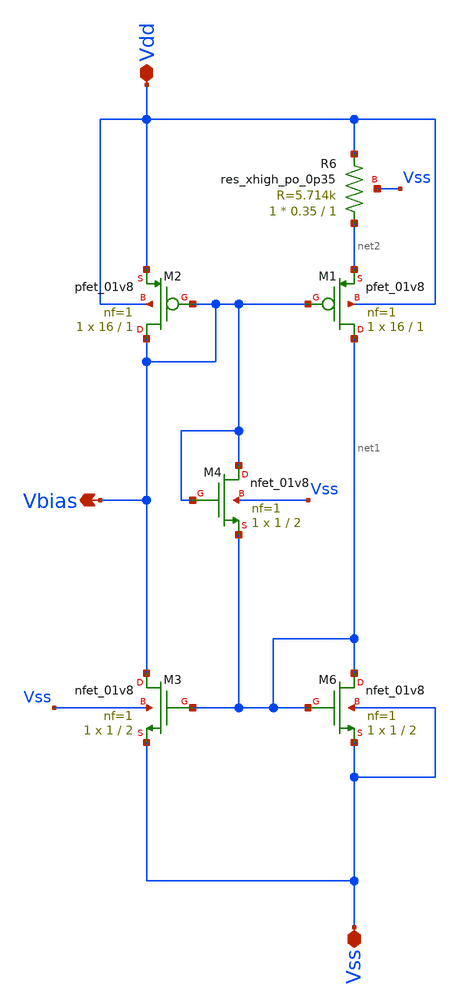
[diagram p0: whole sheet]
** sch_path: Circuits/Examples/OpAmp/GmBiasP.sch
**.subckt GmBiasP Vss Vdd Vbias
*.iopin Vss
*.iopin Vdd
*.opin Vbias
XM6 net1 net1 Vss Vss sky130_fd_pr__nfet_01v8 L=2 W=1 nf=1 ad='int((nf+1)/2) * W/nf * 0.29' as='int((nf+2)/2) * W/nf * 0.29'
+ pd='2*int((nf+1)/2) * (W/nf + 0.29)' ps='2*int((nf+2)/2) * (W/nf + 0.29)' nrd='0.29 / W' nrs='0.29 / W'
+ sa=0 sb=0 sd=0 mult=1 m=1
XM2 Vbias Vbias Vdd Vdd sky130_fd_pr__pfet_01v8 L=1 W=16 nf=1 ad='int((nf+1)/2) * W/nf * 0.29' as='int((nf+2)/2) * W/nf * 0.29'
+ pd='2*int((nf+1)/2) * (W/nf + 0.29)' ps='2*int((nf+2)/2) * (W/nf + 0.29)' nrd='0.29 / W' nrs='0.29 / W'
+ sa=0 sb=0 sd=0 mult=1 m=1
XM1 net1 Vbias net2 Vdd sky130_fd_pr__pfet_01v8 L=1 W=16 nf=1 ad='int((nf+1)/2) * W/nf * 0.29' as='int((nf+2)/2) * W/nf * 0.29'
+ pd='2*int((nf+1)/2) * (W/nf + 0.29)' ps='2*int((nf+2)/2) * (W/nf + 0.29)' nrd='0.29 / W' nrs='0.29 / W'
+ sa=0 sb=0 sd=0 mult=1 m=1
XM3 Vbias net1 Vss Vss sky130_fd_pr__nfet_01v8 L=2 W=1 nf=1 ad='int((nf+1)/2) * W/nf * 0.29' as='int((nf+2)/2) * W/nf * 0.29'
+ pd='2*int((nf+1)/2) * (W/nf + 0.29)' ps='2*int((nf+2)/2) * (W/nf + 0.29)' nrd='0.29 / W' nrs='0.29 / W'
+ sa=0 sb=0 sd=0 mult=1 m=1
XR6 net2 Vdd Vss sky130_fd_pr__res_xhigh_po_0p35 L=1 mult=1 m=1
XM4 Vbias Vbias net1 Vss sky130_fd_pr__nfet_01v8 L=2 W=1 nf=1 ad='int((nf+1)/2) * W/nf * 0.29' as='int((nf+2)/2) * W/nf * 0.29'
+ pd='2*int((nf+1)/2) * (W/nf + 0.29)' ps='2*int((nf+2)/2) * (W/nf + 0.29)' nrd='0.29 / W' nrs='0.29 / W'
+ sa=0 sb=0 sd=0 mult=1 m=1
**.ends
.end
